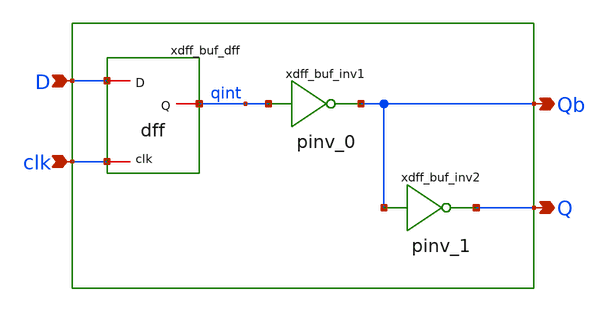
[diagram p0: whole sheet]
** sch_path: sram_4_16_scn4m/dff_buf_0.sch
**.subckt dff_buf_0 D Q Qb clk
*.ipin D
*.opin Q
*.opin Qb
*.ipin clk
xdff_buf_dff D qint clk vdd gnd dff
xdff_buf_inv1 qint Qb vdd gnd pinv_0
xdff_buf_inv2 Qb Q vdd gnd pinv_1
**.ends
.end
